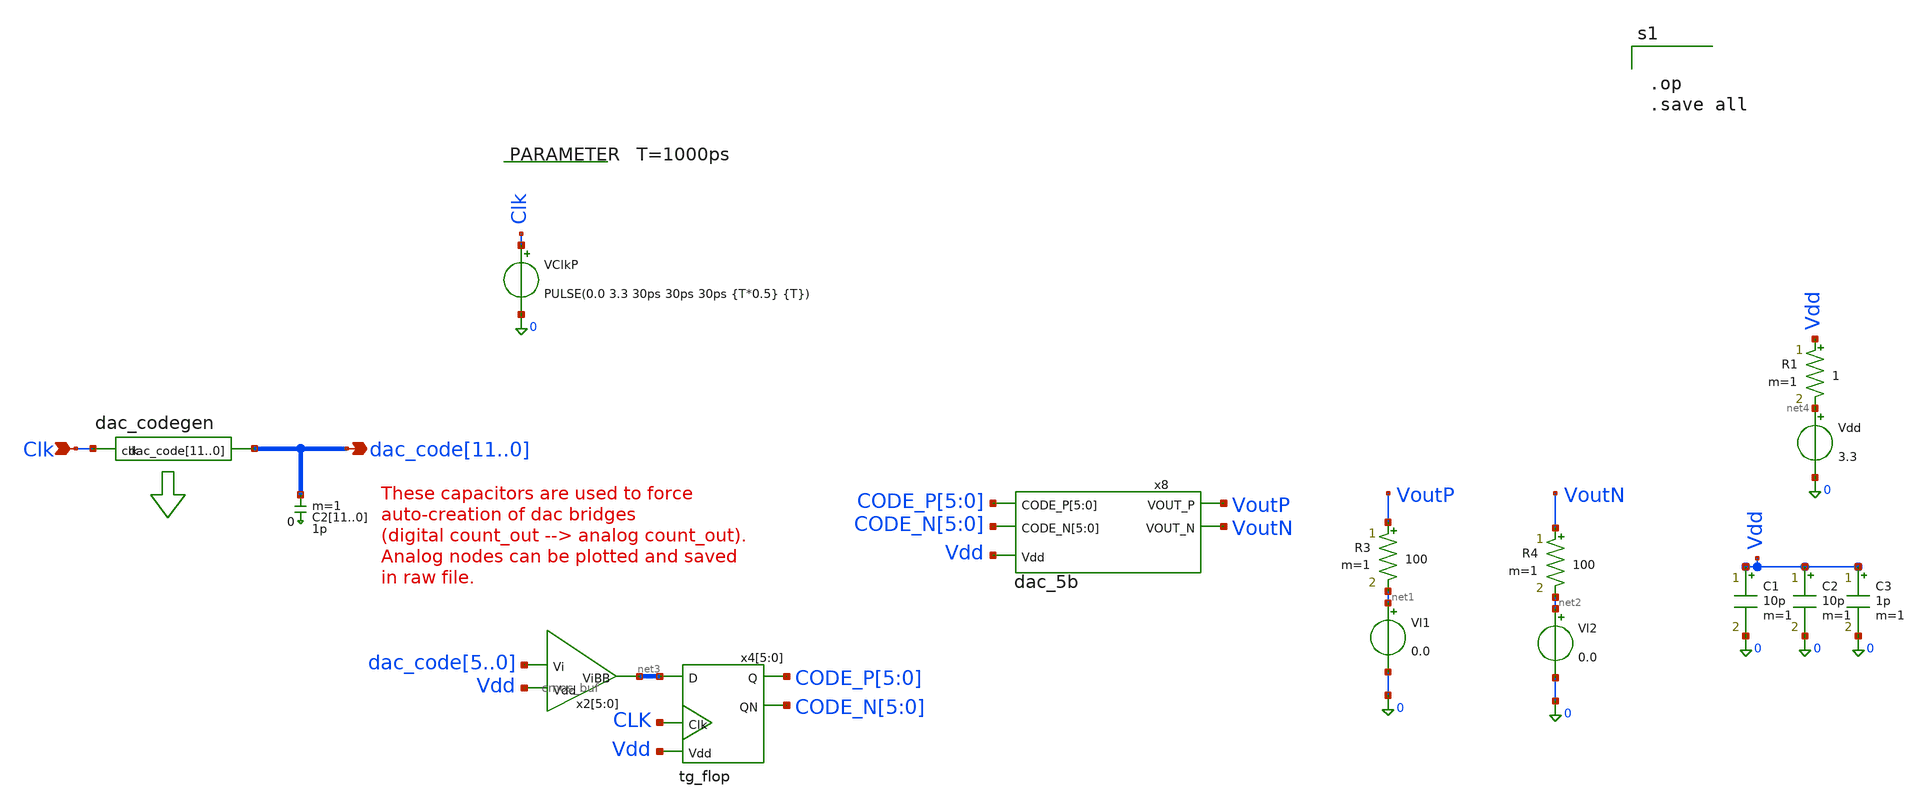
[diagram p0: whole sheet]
** sch_path: blocks/dac/test/test_dac_res_5b.sch
**.subckt test_dac_res_5b
*+ dac_code11,dac_code10,dac_code9,dac_code8,dac_code7,dac_code6,dac_code5,dac_code4,dac_code3,dac_code2,dac_code1,dac_code0 Clk
*.opin
*+ dac_code11,dac_code10,dac_code9,dac_code8,dac_code7,dac_code6,dac_code5,dac_code4,dac_code3,dac_code2,dac_code1,dac_code0
*.ipin Clk
Vdd net4 0 3.3
.save i(vdd)
VClkP Clk 0 PULSE(0.0 3.3 30ps 30ps 30ps {T*0.5} {T})
.save i(vclkp)
R3 VoutP net1 100 m=1
R4 VoutN net2 100 m=1
Vl1 net1 0 0.0
.save i(vl1)
Vl2 net2 0 0.0
.save i(vl2)
C211 dac_code11 0 1p m=1
C210 dac_code10 0 1p m=1
C29 dac_code9 0 1p m=1
C28 dac_code8 0 1p m=1
C27 dac_code7 0 1p m=1
C26 dac_code6 0 1p m=1
C25 dac_code5 0 1p m=1
C24 dac_code4 0 1p m=1
C23 dac_code3 0 1p m=1
C22 dac_code2 0 1p m=1
C21 dac_code1 0 1p m=1
C20 dac_code0 0 1p m=1
a1 [ Clk ] [ dac_code11 dac_code10 dac_code9 dac_code8 dac_code7 dac_code6 dac_code5 dac_code4
+ dac_code3 dac_code2 dac_code1 dac_code0 ] dac_codegen
.param T=1000ps
R1 Vdd net4 1 m=1
C1 Vdd 0 10p m=1
C2 Vdd 0 10p m=1
C3 Vdd 0 1p m=1
x8 Vdd VoutP CODE_P[5] CODE_P[4] CODE_P[3] CODE_P[2] CODE_P[1] CODE_P[0] VoutN CODE_N[5] CODE_N[4]
+ CODE_N[3] CODE_N[2] CODE_N[1] CODE_N[0] dac_5b
x2[5] net3[5] dac_code5 Vdd cmos_buf
x2[4] net3[4] dac_code4 Vdd cmos_buf
x2[3] net3[3] dac_code3 Vdd cmos_buf
x2[2] net3[2] dac_code2 Vdd cmos_buf
x2[1] net3[1] dac_code1 Vdd cmos_buf
x2[0] net3[0] dac_code0 Vdd cmos_buf
x4[5] Vdd CLK CODE_P[5] net3[5] CODE_N[5] tg_flop
x4[4] Vdd CLK CODE_P[4] net3[4] CODE_N[4] tg_flop
x4[3] Vdd CLK CODE_P[3] net3[3] CODE_N[3] tg_flop
x4[2] Vdd CLK CODE_P[2] net3[2] CODE_N[2] tg_flop
x4[1] Vdd CLK CODE_P[1] net3[1] CODE_N[1] tg_flop
x4[0] Vdd CLK CODE_P[0] net3[0] CODE_N[0] tg_flop
**** begin user architecture code



.save all

.param VCC=3.3
.control

pre_set auto_bridge_d_out =   ( ".model auto_dac dac_bridge(out_low=0.0 out_high=3.3 out_undef=1.8
+ input_load=1E-15 t_rise=50p t_fall=50p)"   "auto_bridge%d [ %s ] [ %s ] auto_dac" )

tran 10p 200ns

* plot VU1syncP+6 VU1syncN+6 VU2syncP+6 VU2syncN+6 VgN+12 VgP Dm ClkP+18 ClkN+18 i(Vl1)*5E4-6
*+ i(Vl2)*5E4-6 (i(Vl1)-i(Vl2))*5E4-12
* plot ClkP+6 ClkN+6 VU0in VB1in VU0syncP-6 VU0syncN-12 VB1syncP-6 VB1syncN-12
* plot Vout1P+15E-3 Vout1N+15E-3 Vout1P-Vout1N
* plot ClkP+5 ClkN+5 VB3syncP VB3syncN VB3bufP-5 VB3bufN-5 x1.Vg1P-10 x1.Vg1N-10 x2.Vg1P-15
*+ x2.Vg1N-15

plot i(VoutB3P)-i(VoutB3N) i(VoutU0P)-i(VoutU0N) i(VoutB4P)-i(VoutB4N) i(VoutB2P)-i(VoutB2N)
+ i(VoutB1P)-i(VoutB1N) xlimit 6.1ns 6.5ns

* plot VB1syncP VB1syncN-6 VB4syncN-6 VU0bufP-12 VB1bufP-12 VB4bufP-12 VU0bufN-18 VB1bufN-18
*+ VB4bufN-18
* plot i(Vl1)-i(Vl2) i(Vl1)+100E-6 i(Vl2)+100E-6
plot i(Vl1)-i(Vl2)
let diff = i(Vl1)-i(Vl2)

* plot pulseP diff/560E-6*5 fghz xlimit 12ns 20ns
* plot pulseP diff/560E-6*5 fghz xlimit 0ns 8ns
* plot pulseP fghz

* plot dac_code0 dac_code1
* plot dac_code0 dac_code5


plot x7.Vshift x7.x1.vfil x7.x1.vref

* plot i(VoutB3P)+100E-6 i(VoutB3N)+100E-6 i(VoutB3P)-i(VoutB3N) i(VoutB3N)+i(VoutB3P)
*+ i(v.x1.Vcrr1)-200E-6 i(v.x1.Vcrr2)-200E-6
* plot i(Vl1) VB1in/5E4+200E-6 VU0in/5E4+200E-6
wrdata /foss/designs/dac/waveform_5bit.csv Clk dac_code0 dac_code1 dac_code2 dac_code3 dac_code4
+ i(Vl1) i(Vl2)  i(Vl1)-i(Vl2)
.endc





.op
.save all




.include /foss/pdks/gf180mcuD/libs.tech/ngspice/design.ngspice typical
.lib /foss/pdks/gf180mcuD/libs.tech/ngspice/sm141064.ngspice typical
.lib /foss/pdks/gf180mcuD/libs.tech/ngspice/sm141064.ngspice res_typical
.lib /foss/pdks/gf180mcuD/libs.tech/ngspice/sm141064.ngspice mimcap_typical


**** end user architecture code
**.ends
**** begin user architecture code
.model dac_codegen d_cosim simulation="/foss/designs/dac/dac_codegen.so"
**** end user architecture code
.end
